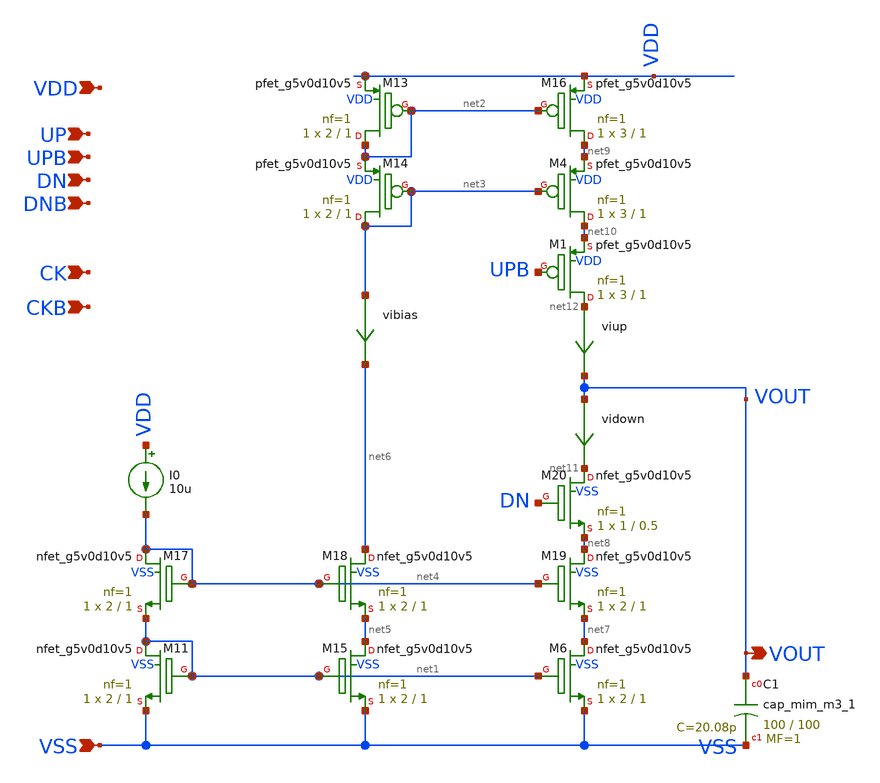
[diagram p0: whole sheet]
** sch_path: xschem/pll_cp_delta_hv.sch
**.subckt pll_cp_delta_hv VOUT VSS UP DNB CK CKB VDD DN UPB
*.opin VOUT
*.ipin VSS
*.ipin UP
*.ipin DNB
*.ipin CK
*.ipin CKB
*.ipin VDD
*.ipin DN
*.ipin UPB
XC1 VOUT VSS sky130_fd_pr__cap_mim_m3_1 W=100 L=100 MF=1 m=1
vibias net3 net6 0
.save i(vibias)
XM16 net9 net2 VDD VDD sky130_fd_pr__pfet_g5v0d10v5 L=1 W=3 nf=1 ad='int((nf+1)/2) * W/nf * 0.29' as='int((nf+2)/2) * W/nf * 0.29'
+ pd='2*int((nf+1)/2) * (W/nf + 0.29)' ps='2*int((nf+2)/2) * (W/nf + 0.29)' nrd='0.29 / W' nrs='0.29 / W'
+ sa=0 sb=0 sd=0 mult=1 m=1
XM13 net2 net2 VDD VDD sky130_fd_pr__pfet_g5v0d10v5 L=1 W=2 nf=1 ad='int((nf+1)/2) * W/nf * 0.29' as='int((nf+2)/2) * W/nf * 0.29'
+ pd='2*int((nf+1)/2) * (W/nf + 0.29)' ps='2*int((nf+2)/2) * (W/nf + 0.29)' nrd='0.29 / W' nrs='0.29 / W'
+ sa=0 sb=0 sd=0 mult=1 m=1
XM14 net3 net3 net2 VDD sky130_fd_pr__pfet_g5v0d10v5 L=1 W=2 nf=1 ad='int((nf+1)/2) * W/nf * 0.29' as='int((nf+2)/2) * W/nf * 0.29'
+ pd='2*int((nf+1)/2) * (W/nf + 0.29)' ps='2*int((nf+2)/2) * (W/nf + 0.29)' nrd='0.29 / W' nrs='0.29 / W'
+ sa=0 sb=0 sd=0 mult=1 m=1
I0 VDD net4 10u
XM11 net1 net1 VSS VSS sky130_fd_pr__nfet_g5v0d10v5 L=1 W=2 nf=1 ad='int((nf+1)/2) * W/nf * 0.29' as='int((nf+2)/2) * W/nf * 0.29'
+ pd='2*int((nf+1)/2) * (W/nf + 0.29)' ps='2*int((nf+2)/2) * (W/nf + 0.29)' nrd='0.29 / W' nrs='0.29 / W'
+ sa=0 sb=0 sd=0 mult=1 m=1
XM17 net4 net4 net1 VSS sky130_fd_pr__nfet_g5v0d10v5 L=1 W=2 nf=1 ad='int((nf+1)/2) * W/nf * 0.29' as='int((nf+2)/2) * W/nf * 0.29'
+ pd='2*int((nf+1)/2) * (W/nf + 0.29)' ps='2*int((nf+2)/2) * (W/nf + 0.29)' nrd='0.29 / W' nrs='0.29 / W'
+ sa=0 sb=0 sd=0 mult=1 m=1
XM15 net5 net1 VSS VSS sky130_fd_pr__nfet_g5v0d10v5 L=1 W=2 nf=1 ad='int((nf+1)/2) * W/nf * 0.29' as='int((nf+2)/2) * W/nf * 0.29'
+ pd='2*int((nf+1)/2) * (W/nf + 0.29)' ps='2*int((nf+2)/2) * (W/nf + 0.29)' nrd='0.29 / W' nrs='0.29 / W'
+ sa=0 sb=0 sd=0 mult=1 m=1
XM18 net6 net4 net5 VSS sky130_fd_pr__nfet_g5v0d10v5 L=1 W=2 nf=1 ad='int((nf+1)/2) * W/nf * 0.29' as='int((nf+2)/2) * W/nf * 0.29'
+ pd='2*int((nf+1)/2) * (W/nf + 0.29)' ps='2*int((nf+2)/2) * (W/nf + 0.29)' nrd='0.29 / W' nrs='0.29 / W'
+ sa=0 sb=0 sd=0 mult=1 m=1
XM6 net7 net1 VSS VSS sky130_fd_pr__nfet_g5v0d10v5 L=1 W=2 nf=1 ad='int((nf+1)/2) * W/nf * 0.29' as='int((nf+2)/2) * W/nf * 0.29'
+ pd='2*int((nf+1)/2) * (W/nf + 0.29)' ps='2*int((nf+2)/2) * (W/nf + 0.29)' nrd='0.29 / W' nrs='0.29 / W'
+ sa=0 sb=0 sd=0 mult=1 m=1
XM19 net8 net4 net7 VSS sky130_fd_pr__nfet_g5v0d10v5 L=1 W=2 nf=1 ad='int((nf+1)/2) * W/nf * 0.29' as='int((nf+2)/2) * W/nf * 0.29'
+ pd='2*int((nf+1)/2) * (W/nf + 0.29)' ps='2*int((nf+2)/2) * (W/nf + 0.29)' nrd='0.29 / W' nrs='0.29 / W'
+ sa=0 sb=0 sd=0 mult=1 m=1
XM20 net11 DN net8 VSS sky130_fd_pr__nfet_g5v0d10v5 L=0.5 W=1 nf=1 ad='int((nf+1)/2) * W/nf * 0.29' as='int((nf+2)/2) * W/nf * 0.29'
+ pd='2*int((nf+1)/2) * (W/nf + 0.29)' ps='2*int((nf+2)/2) * (W/nf + 0.29)' nrd='0.29 / W' nrs='0.29 / W'
+ sa=0 sb=0 sd=0 mult=1 m=1
XM4 net10 net3 net9 VDD sky130_fd_pr__pfet_g5v0d10v5 L=1 W=3 nf=1 ad='int((nf+1)/2) * W/nf * 0.29' as='int((nf+2)/2) * W/nf * 0.29'
+ pd='2*int((nf+1)/2) * (W/nf + 0.29)' ps='2*int((nf+2)/2) * (W/nf + 0.29)' nrd='0.29 / W' nrs='0.29 / W'
+ sa=0 sb=0 sd=0 mult=1 m=1
viup net12 VOUT 0
.save i(viup)
vidown VOUT net11 0
.save i(vidown)
XM1 net12 UPB net10 VDD sky130_fd_pr__pfet_g5v0d10v5 L=1 W=3 nf=1 ad='int((nf+1)/2) * W/nf * 0.29' as='int((nf+2)/2) * W/nf * 0.29'
+ pd='2*int((nf+1)/2) * (W/nf + 0.29)' ps='2*int((nf+2)/2) * (W/nf + 0.29)' nrd='0.29 / W' nrs='0.29 / W'
+ sa=0 sb=0 sd=0 mult=1 m=1
**.ends
.end
